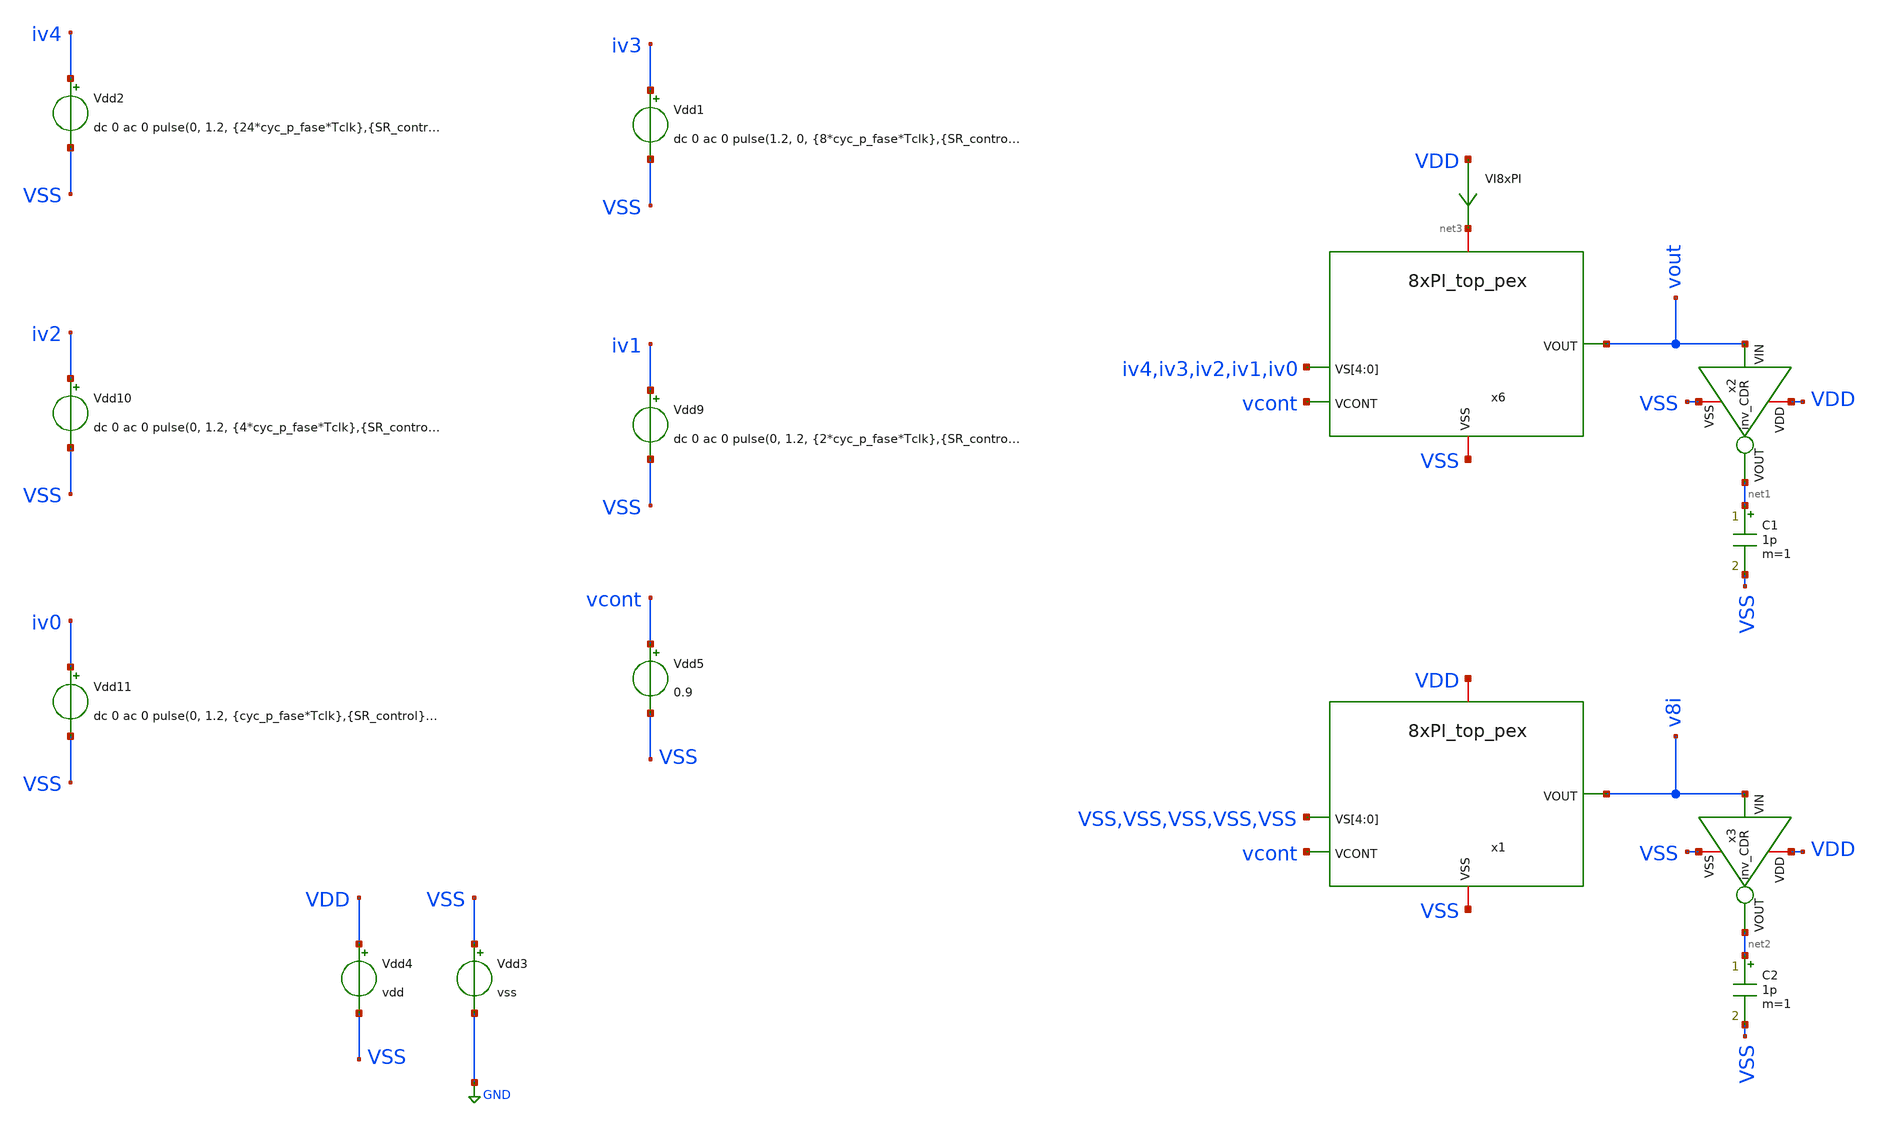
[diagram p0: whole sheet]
** sch_path: CDR4176-main/testbenches/tran/xschem/tb_8xPI_top_pex.sch
**.subckt tb_8xPI_top_pex
Vdd9 iv1 VSS dc 0 ac 0 pulse(0, 1.2, {2*cyc_p_fase*Tclk},{SR_control},{SR_control}, {2*cyc_p_fase*Tclk},
+ {4*cyc_p_fase*Tclk})
Vdd10 iv2 VSS dc 0 ac 0 pulse(0, 1.2, {4*cyc_p_fase*Tclk},{SR_control},{SR_control}, {4*cyc_p_fase*Tclk},
+ {8*cyc_p_fase*Tclk})
Vdd11 iv0 VSS dc 0 ac 0 pulse(0, 1.2, {cyc_p_fase*Tclk},{SR_control},{SR_control}, {cyc_p_fase*Tclk},
+ {2*cyc_p_fase*Tclk})
Vdd1 iv3 VSS dc 0 ac 0 pulse(1.2, 0, {8*cyc_p_fase*Tclk},{SR_control},{SR_control}, {8*cyc_p_fase*Tclk},
+ {16*cyc_p_fase*Tclk})
Vdd2 iv4 VSS dc 0 ac 0 pulse(0, 1.2, {24*cyc_p_fase*Tclk},{SR_control},{SR_control}, {16*cyc_p_fase*Tclk},
+ {40*cyc_p_fase*Tclk})
Vdd4 VDD VSS vdd
Vdd3 VSS GND vss
Vdd5 vcont VSS 0.9
C1 net1 VSS 1p m=1
C2 net2 VSS 1p m=1
VI8xPI VDD net3 0
.save i(vi8xpi)
x6 net3 iv4 iv3 iv2 iv1 iv0 vout vcont VSS 8xPI_top_pex
x1 VDD VSS VSS VSS VSS VSS v8i vcont VSS 8xPI_top_pex
x2 VDD net1 vout VSS inv_CDR
x3 VDD net2 v8i VSS inv_CDR
**** begin user architecture code



* Circuit Parameters
.param vdd = 1.2
.param vss = 0.0
.param Tclk = 1375p
.param cyc_p_fase = 4
.param SR_control=110p
.options TEMP = 27.0
.OPTION RSHUNT=1e10

* Include Models
.lib cornerMOSlv.lib mos_tt
.inc /foss/designs/IHP__CDR4176/CDR4176-main/netlist/pex/8xPI_top_pex.spice


* OP Parameters & Singals to save
.save V(vout) V(v8i) I(VI8xPI)

*Simulations
.control
	set output_path = ../../verification/python/
	set ngdebug
	set verbose
	tran 5PS 221NS
	set filetype = ascii
        write {$output_path}tran_linearity_8xPI_top_pex.raw
.endc
.end

**** end user architecture code
**.ends

* expanding   symbol:  inv_CDR/inv_CDR.sym # of pins=4
** sym_path: CDR4176-main/schematic/xschem/inv_CDR/inv_CDR.sym
** sch_path: CDR4176-main/schematic/xschem/inv_CDR/inv_CDR.sch
.subckt inv_CDR VDD VOUT VIN VSS
*.iopin VDD
*.iopin VSS
*.opin VOUT
*.ipin VIN
XM2 VOUT VIN VDD VDD sg13_lv_pmos w=0.15u l=0.13u ng=1 m=1 mm_ok=1
XM1 VOUT VIN VSS VSS sg13_lv_nmos w=0.15u l=0.13u ng=1 m=1 mm_ok=1
.ends

.GLOBAL GND
.end
